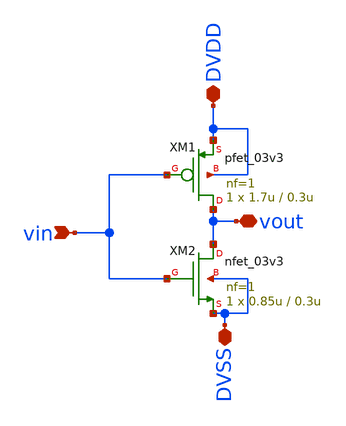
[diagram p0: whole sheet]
** sch_path: designs/emily_testing/inv1.sch
**.subckt inv1 vin vout DVDD DVSS
*.ipin vin
*.iopin vout
*.iopin DVDD
*.iopin DVSS
XM1 vout vin DVDD DVDD pfet_03v3 L=0.3u W=1.7u nf=1 ad='int((nf+1)/2) * W/nf * 0.18u' as='int((nf+2)/2) * W/nf * 0.18u'
+ pd='2*int((nf+1)/2) * (W/nf + 0.18u)' ps='2*int((nf+2)/2) * (W/nf + 0.18u)' nrd='0.18u / W' nrs='0.18u / W'
+ sa=0 sb=0 sd=0 m=1
XM2 vout vin DVSS DVSS nfet_03v3 L=0.3u W=0.85u nf=1 ad='int((nf+1)/2) * W/nf * 0.18u' as='int((nf+2)/2) * W/nf * 0.18u'
+ pd='2*int((nf+1)/2) * (W/nf + 0.18u)' ps='2*int((nf+2)/2) * (W/nf + 0.18u)' nrd='0.18u / W' nrs='0.18u / W'
+ sa=0 sb=0 sd=0 m=1
**** begin user architecture code
lab=#net4

**** end user architecture code
**.ends
.end
